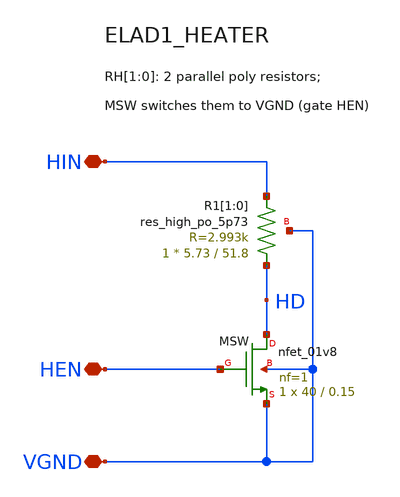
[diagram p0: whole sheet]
** sch_path: cells/ELAD1_HEATER/schematic/ELAD1_HEATER.sch
**.subckt ELAD1_HEATER HIN HEN VGND
*.iopin HIN
*.iopin HEN
*.iopin VGND
XMSW HD HEN VGND VGND sky130_fd_pr__nfet_01v8 L=0.15 W=40 nf=1 ad='int((1 + 1)/2) * 40 / 1 * 0.29' as='int((1 + 2)/2) * 40 / 1 * 0.29'
+ pd='2*int((1 + 1)/2) * (40 / 1 + 0.29)' ps='2*int((1 + 2)/2) * (40 / 1 + 0.29)' nrd='0.29 / 40 ' nrs='0.29 / 40 '
+ sa=0 sb=0 sd=0 mult=1 m=1
XR1[1] HD HIN VGND sky130_fd_pr__res_high_po_5p73 L=51.8 mult=1 m=1
XR1[0] HD HIN VGND sky130_fd_pr__res_high_po_5p73 L=51.8 mult=1 m=1
**.ends
.end
